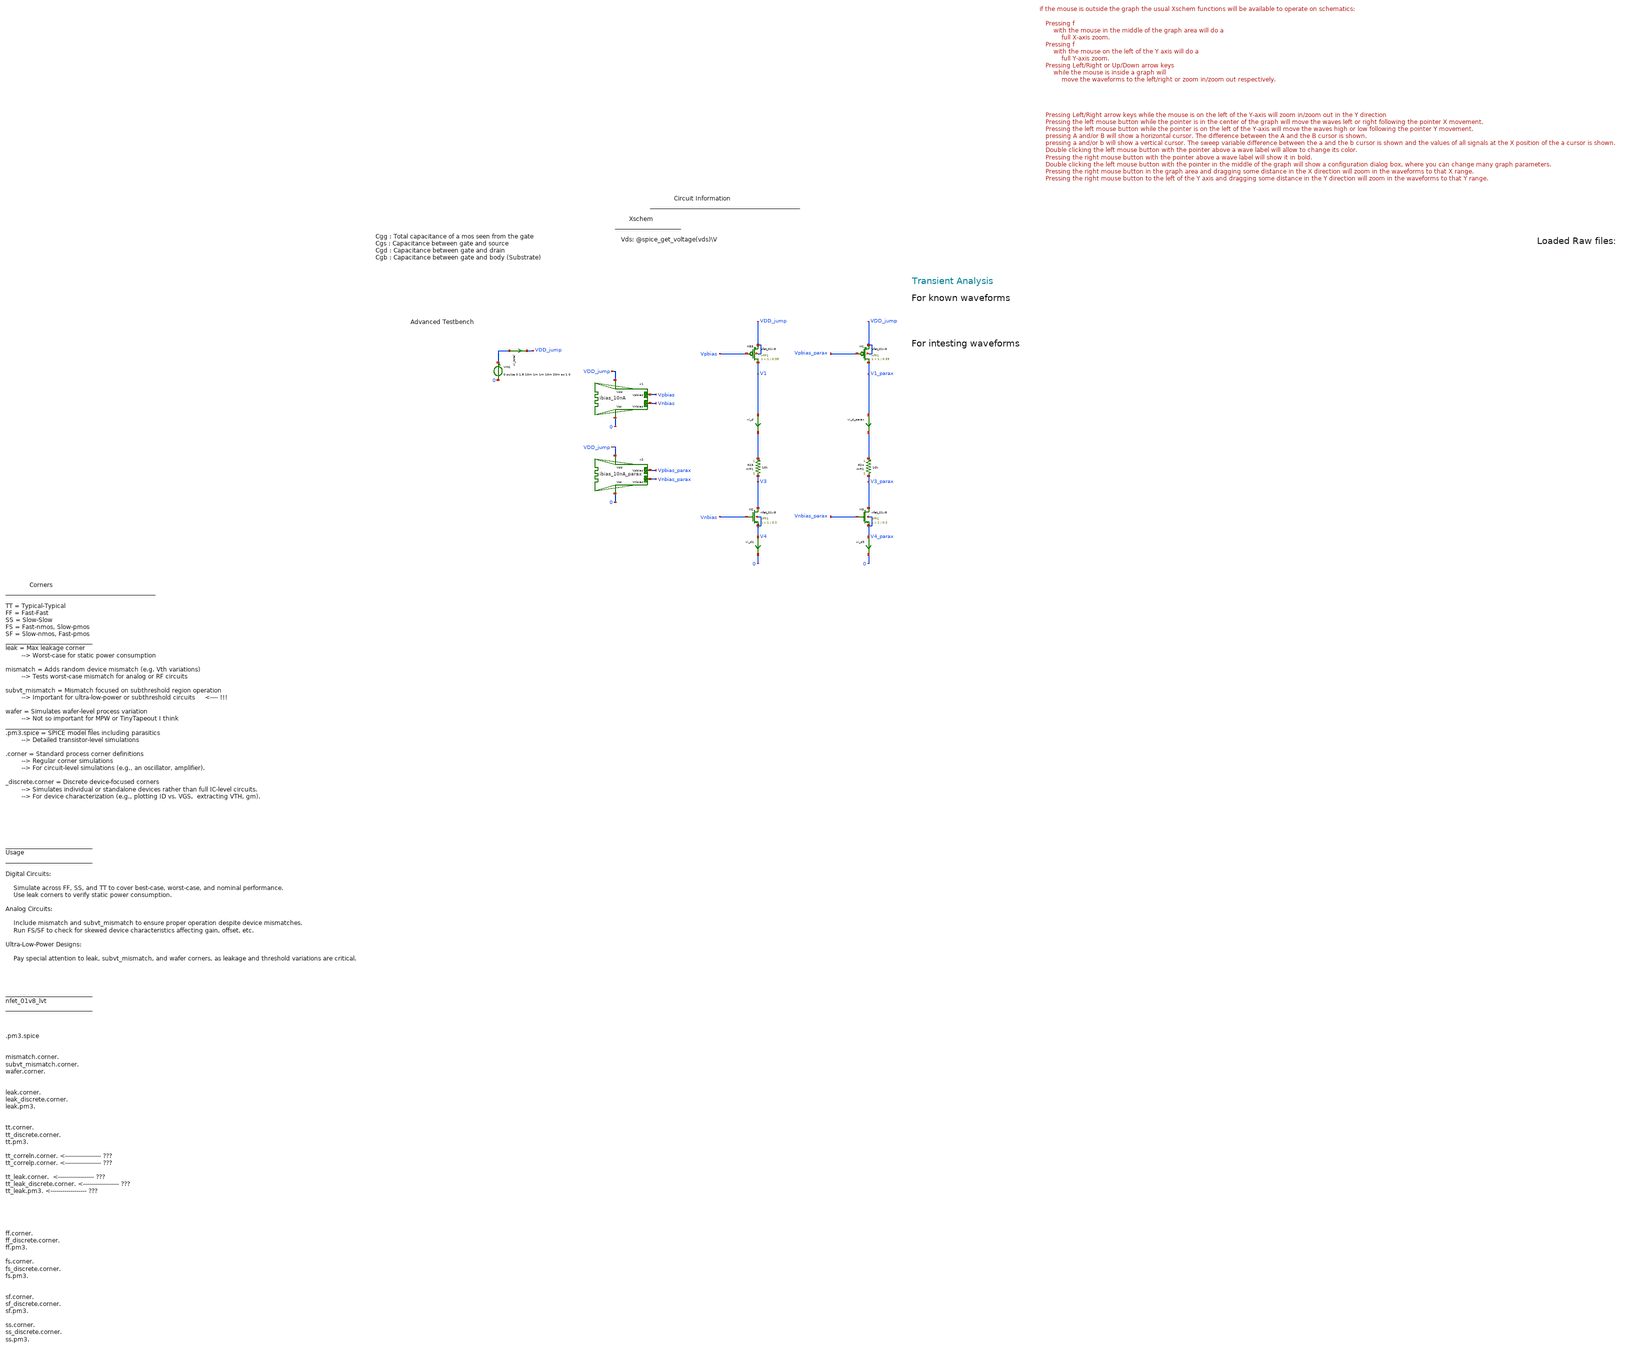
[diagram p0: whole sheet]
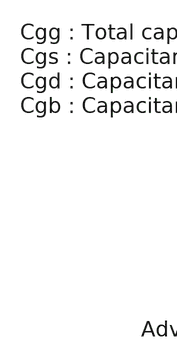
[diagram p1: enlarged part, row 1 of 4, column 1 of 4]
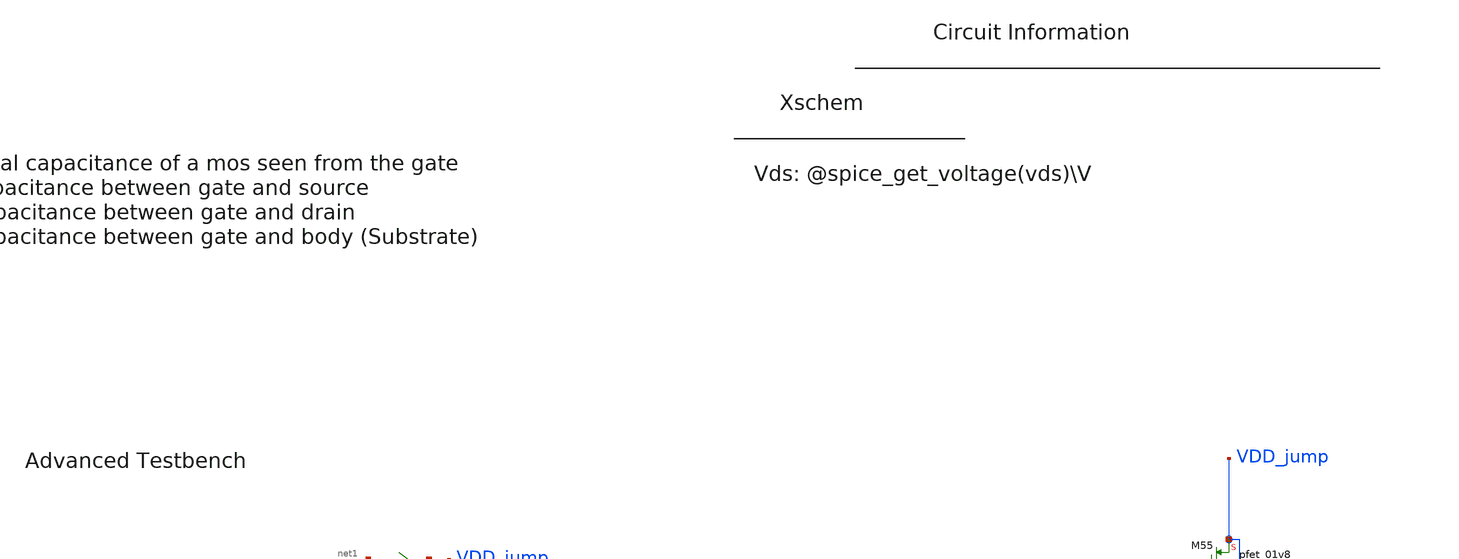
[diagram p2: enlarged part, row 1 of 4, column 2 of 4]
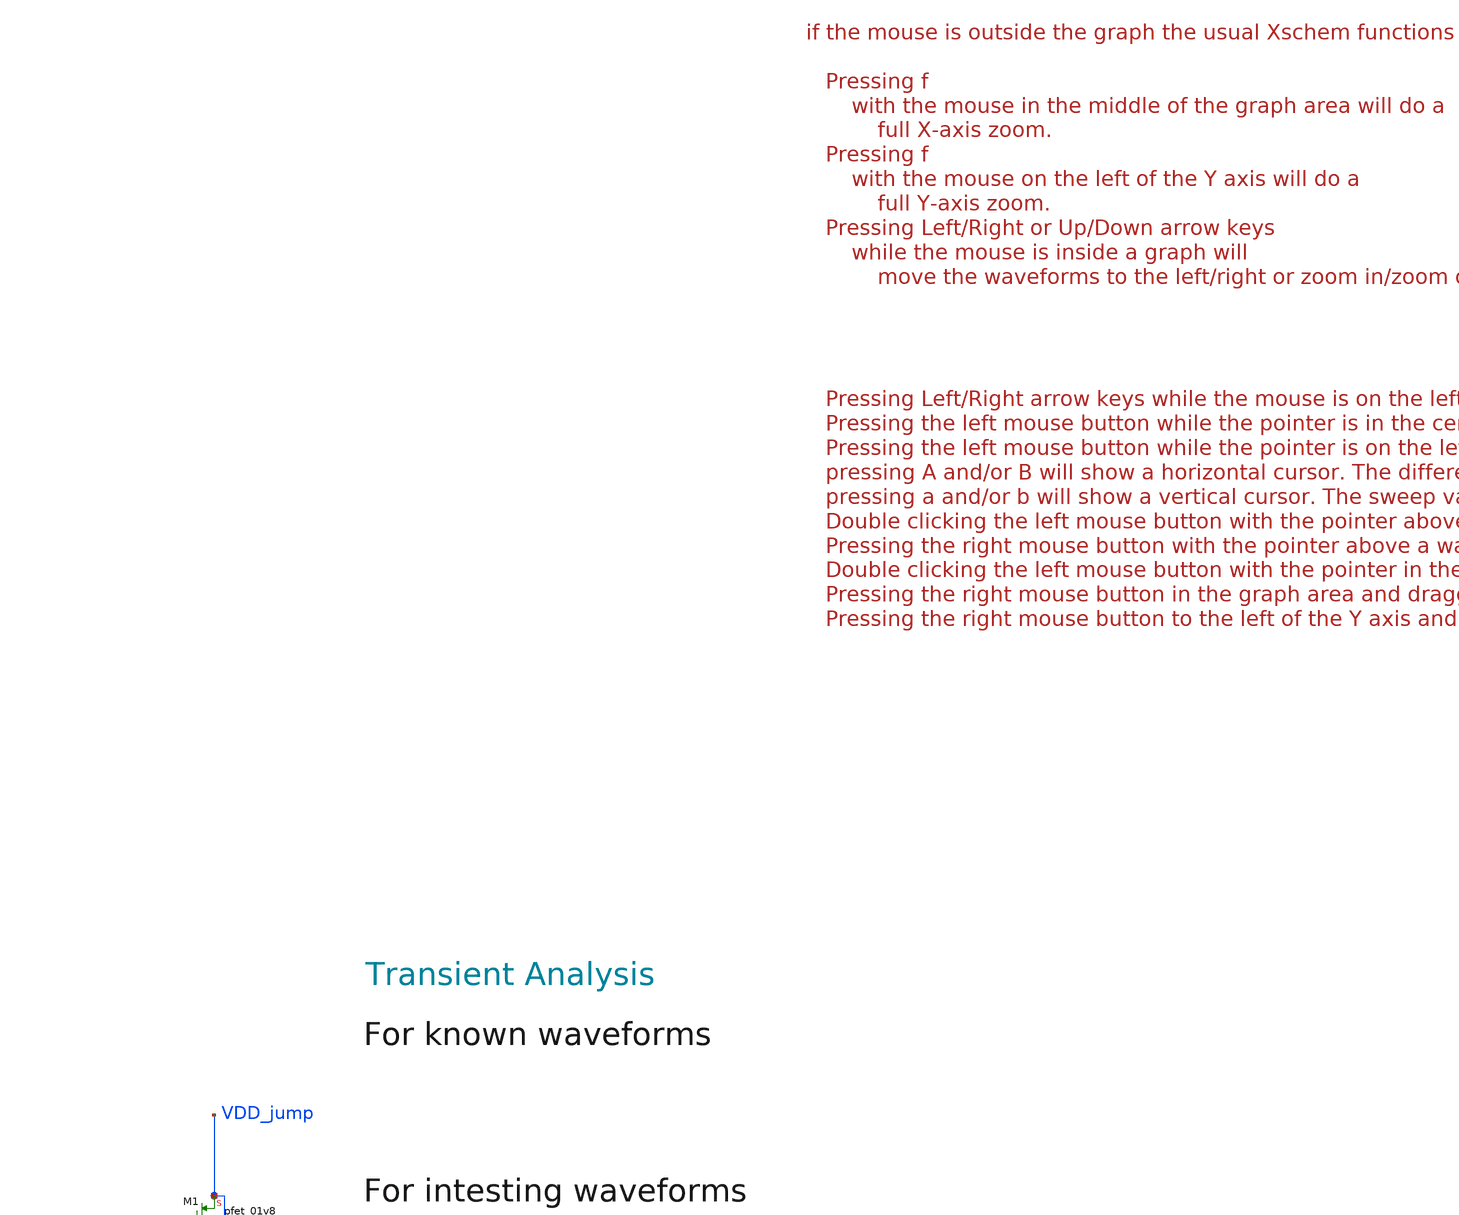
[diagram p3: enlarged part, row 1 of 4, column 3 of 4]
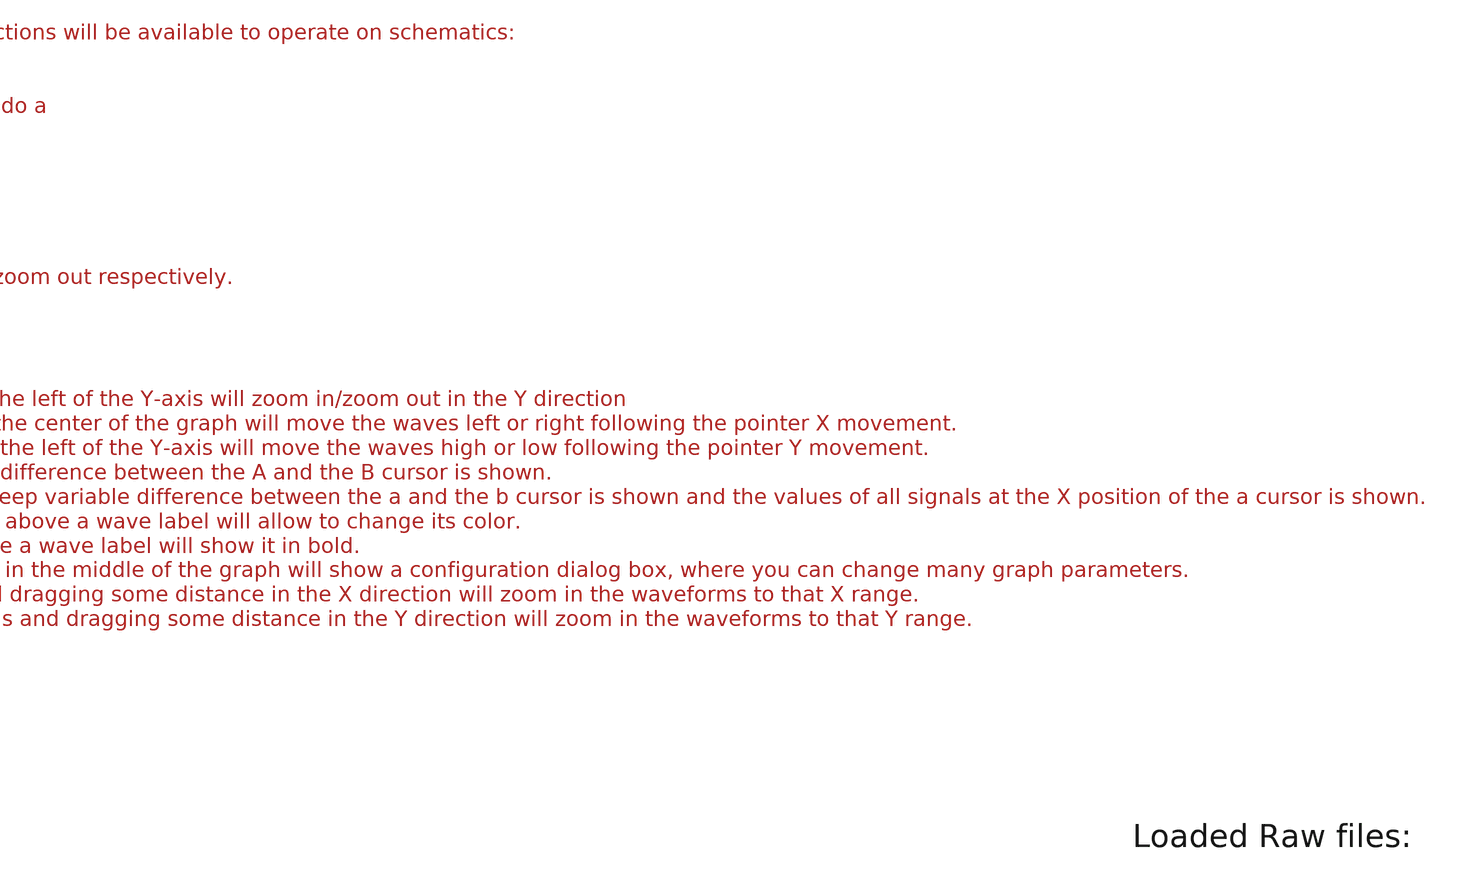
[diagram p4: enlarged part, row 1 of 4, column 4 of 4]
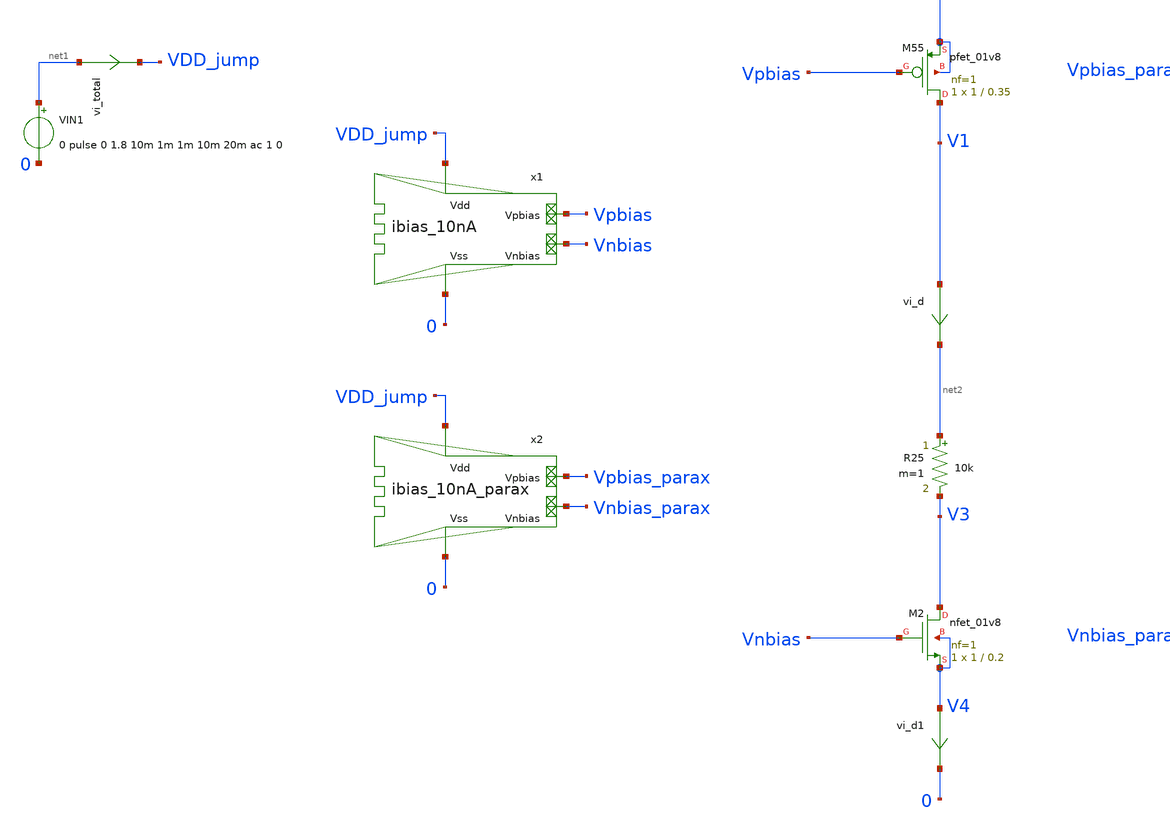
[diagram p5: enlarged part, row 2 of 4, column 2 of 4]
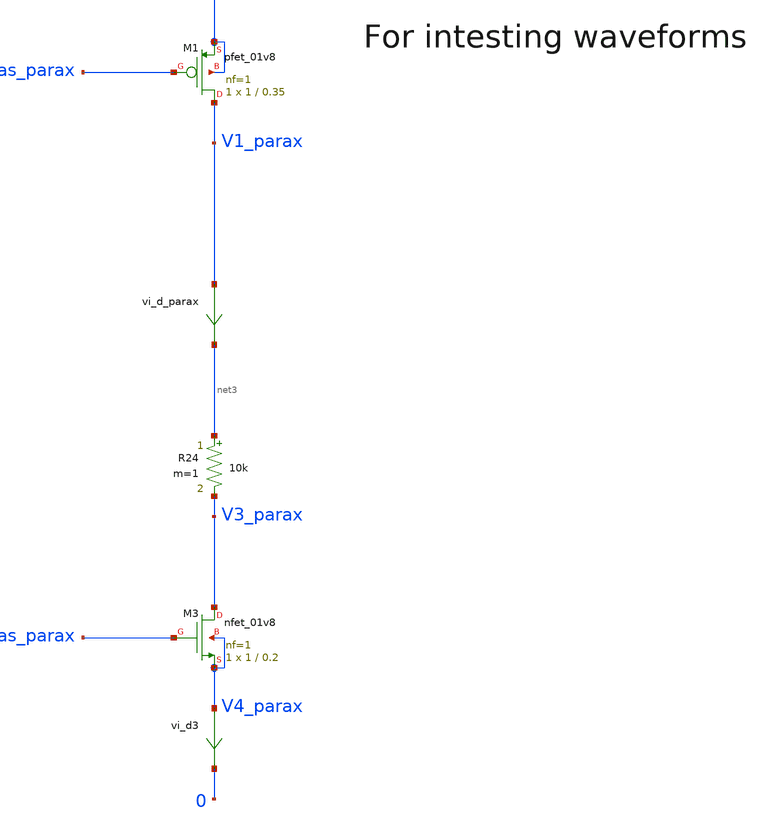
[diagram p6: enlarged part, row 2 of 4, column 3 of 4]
** sch_path: tt10-hdl/tt_um_test_commit/xschem/T2/biasGen/A_tt10_10nA/ibias_10nA_PARAX_tran_tb.sch
* Copyright (C) 1998-2024 Stefan Frederik Schippers
* This program is free software; you can redistribute it and/or modify
* it under the terms of the GNU General Public License as published by
* the Free Software Foundation; either version 2 of the License, or
* (at your option) any later version.
* This program is distributed in the hope that it will be useful,
* but WITHOUT ANY WARRANTY; without even the implied warranty of
* MERCHANTABILITY or FITNESS FOR A PARTICULAR PURPOSE.  See the
* GNU General Public License for more details.
* You should have received a copy of the GNU General Public License
* along with this program; if not, write to the Free Software
**.subckt ibias_10nA_PARAX_tran_tb
VIN1 net1 0 0 pulse 0 1.8 10m 1m 1m 10m 20m ac 1 0
vi_total net1 VDD_jump 0
.save i(vi_total)
vi_d V1 net2 0
.save i(vi_d)
x1 VDD_jump 0 Vnbias Vpbias ibias_10nA
XM55 V1 Vpbias VDD_jump VDD_jump sky130_fd_pr__pfet_01v8 L=0.35 W=1 nf=1 ad='int((nf+1)/2) * W/nf * 0.29'
+ as='int((nf+2)/2) * W/nf * 0.29' pd='2*int((nf+1)/2) * (W/nf + 0.29)' ps='2*int((nf+2)/2) * (W/nf + 0.29)'
+ nrd='0.29 / W' nrs='0.29 / W' sa=0 sb=0 sd=0 mult=1 m=1
R25 net2 V3 10k m=1
XM2 V3 Vnbias V4 V4 sky130_fd_pr__nfet_01v8 L=0.2 W=1 nf=1 ad='int((1 + 1)/2) * 1 / 1 * 0.29' as='int((1 + 2)/2) * 1 / 1 * 0.29'
+ pd='2*int((1 + 1)/2) * (1 / 1 + 0.29)' ps='2*int((1 + 2)/2) * (1 / 1 + 0.29)' nrd='0.29 / 1 ' nrs='0.29 / 1 '
+ sa=0 sb=0 sd=0 mult=1 m=1
vi_d1 V4 0 0
.save i(vi_d1)
vi_d_parax V1_parax net3 0
.save i(vi_d_parax)
XM1 V1_parax Vpbias_parax VDD_jump VDD_jump sky130_fd_pr__pfet_01v8 L=0.35 W=1 nf=1 ad='int((nf+1)/2) * W/nf * 0.29'
+ as='int((nf+2)/2) * W/nf * 0.29' pd='2*int((nf+1)/2) * (W/nf + 0.29)' ps='2*int((nf+2)/2) * (W/nf + 0.29)'
+ nrd='0.29 / W' nrs='0.29 / W' sa=0 sb=0 sd=0 mult=1 m=1
R24 net3 V3_parax 10k m=1
XM3 V3_parax Vnbias_parax V4_parax V4_parax sky130_fd_pr__nfet_01v8 L=0.2 W=1 nf=1 ad='int((1 + 1)/2) * 1 / 1 * 0.29'
+ as='int((1 + 2)/2) * 1 / 1 * 0.29' pd='2*int((1 + 1)/2) * (1 / 1 + 0.29)' ps='2*int((1 + 2)/2) * (1 / 1 + 0.29)'
+ nrd='0.29 / 1 ' nrs='0.29 / 1 ' sa=0 sb=0 sd=0 mult=1 m=1
vi_d3 V4_parax 0 0
.save i(vi_d3)
x2 VDD_jump 0 Vnbias_parax Vpbias_parax ibias_10nA_parax
**** begin user architecture code



.temp 30

*.option gmin=5n
*.option scale=1e-6
.option wnflag=1
.option savecurrents

.save all
.control
  save all alli
  save @m.xm1.msky130_fd_pr__nfet_01v8[gm]
  save @m.xm1.msky130_fd_pr__nfet_01v8[id]
  save @m.xm1.msky130_fd_pr__nfet_01v8[vgs]

  save @m.xm1.msky130_fd_pr__nfet_01v8[cgg]
  save @m.xm1.msky130_fd_pr__nfet_01v8[cgs]
  save @m.xm1.msky130_fd_pr__nfet_01v8[cgdo]
  save @m.xm1.msky130_fd_pr__nfet_01v8[cgb]

  save @m.xm1.msky130_fd_pr__nfet_01v8[vds]
  save @m.xm1.msky130_fd_pr__nfet_01v8[vdsat]
  save @m.xm1.msky130_fd_pr__nfet_01v8[vth]


  save @m.xm1.msky130_fd_pr__nfet_01v8[leff]
  save @m.xm1.msky130_fd_pr__nfet_01v8[weff]
  save @m.xm1.msky130_fd_pr__nfet_01v8[gds]
  save @m.xm1.msky130_fd_pr__nfet_01v8[l]
  save @m.xm1.msky130_fd_pr__nfet_01v8[w]
  save @m.xm1.msky130_fd_pr__nfet_01v8[gm]
  save @m.xm1.msky130_fd_pr__nfet_01v8[gm]
  save @m.xm1.msky130_fd_pr__nfet_01v8[gm]
  save @m.xm1.msky130_fd_pr__nfet_01v8[gm]
  save @m.xm1.msky130_fd_pr__nfet_01v8[gm]








  tran 1m 50m
  remzerovec
  write nmos_tb_tran.raw

  op
  set appendwrite
  remzerovec
  write nmos_tb_tran.raw






  *quit 0




.endc





** opencircuitdesign pdks install
.lib $::SKYWATER_MODELS/sky130.lib.spice tt
.include $::SKYWATER_STDCELLS/sky130_fd_sc_hd.spice


**** end user architecture code
**.ends

* expanding   symbol:  T2/biasGen/A_tt10_10nA/ibias_10nA.sym # of pins=4
** sym_path: tt10-hdl/tt_um_test_commit/xschem/T2/biasGen/A_tt10_10nA/ibias_10nA.sym
** sch_path: tt10-hdl/tt_um_test_commit/xschem/T2/biasGen/A_tt10_10nA/ibias_10nA.sch
.subckt ibias_10nA Vdd Vss Vnbias Vpbias
*.ipin Vdd
*.ipin Vss
*.opin Vnbias
*.opin Vpbias
XM3 Vpbias Vpbias Vdd Vdd sky130_fd_pr__pfet_01v8 L=0.35 W=0.5 nf=1 ad='int((nf+1)/2) * W/nf * 0.29'
+ as='int((nf+2)/2) * W/nf * 0.29' pd='2*int((nf+1)/2) * (W/nf + 0.29)' ps='2*int((nf+2)/2) * (W/nf + 0.29)'
+ nrd='0.29 / W' nrs='0.29 / W' sa=0 sb=0 sd=0 mult=1 m=1
XM4 Vnbias Vpbias Vdd Vdd sky130_fd_pr__pfet_01v8 L=0.35 W=0.5 nf=1 ad='int((nf+1)/2) * W/nf * 0.29'
+ as='int((nf+2)/2) * W/nf * 0.29' pd='2*int((nf+1)/2) * (W/nf + 0.29)' ps='2*int((nf+2)/2) * (W/nf + 0.29)'
+ nrd='0.29 / W' nrs='0.29 / W' sa=0 sb=0 sd=0 mult=1 m=1
XM5 net2 Vpbias Vdd Vdd sky130_fd_pr__pfet_01v8 L=0.35 W=1 nf=1 ad='int((nf+1)/2) * W/nf * 0.29' as='int((nf+2)/2) * W/nf * 0.29'
+ pd='2*int((nf+1)/2) * (W/nf + 0.29)' ps='2*int((nf+2)/2) * (W/nf + 0.29)' nrd='0.29 / W' nrs='0.29 / W'
+ sa=0 sb=0 sd=0 mult=1 m=1
XM1 Vpbias Vnbias net1 Vss sky130_fd_pr__nfet_01v8 L=0.2 W=0.5 nf=1 ad='int((1 + 1)/2) * 0.5 / 1 * 0.29'
+ as='int((1 + 2)/2) * 0.5 / 1 * 0.29' pd='2*int((1 + 1)/2) * (0.5 / 1 + 0.29)' ps='2*int((1 + 2)/2) * (0.5 / 1 + 0.29)'
+ nrd='0.29 / 0.5 ' nrs='0.29 / 0.5 ' sa=0 sb=0 sd=0 mult=1 m=1
XM2 Vnbias Vnbias Vss Vss sky130_fd_pr__nfet_01v8 L=0.2 W=0.5 nf=1 ad='int((1 + 1)/2) * 0.5 / 1 * 0.29'
+ as='int((1 + 2)/2) * 0.5 / 1 * 0.29' pd='2*int((1 + 1)/2) * (0.5 / 1 + 0.29)' ps='2*int((1 + 2)/2) * (0.5 / 1 + 0.29)'
+ nrd='0.29 / 0.5 ' nrs='0.29 / 0.5 ' sa=0 sb=0 sd=0 mult=1 m=1
XM6 net2 net2 net1 Vss sky130_fd_pr__nfet_01v8 L=0.2 W=1 nf=1 ad='int((1 + 1)/2) * 1 / 1 * 0.29' as='int((1 + 2)/2) * 1 / 1 * 0.29'
+ pd='2*int((1 + 1)/2) * (1 / 1 + 0.29)' ps='2*int((1 + 2)/2) * (1 / 1 + 0.29)' nrd='0.29 / 1 ' nrs='0.29 / 1 '
+ sa=0 sb=0 sd=0 mult=1 m=1
XM7 net1 net2 Vss Vss sky130_fd_pr__nfet_01v8 L=1 W=1 nf=1 ad='int((1 + 1)/2) * 1 / 1 * 0.29' as='int((1 + 2)/2) * 1 / 1 * 0.29'
+ pd='2*int((1 + 1)/2) * (1 / 1 + 0.29)' ps='2*int((1 + 2)/2) * (1 / 1 + 0.29)' nrd='0.29 / 1 ' nrs='0.29 / 1 '
+ sa=0 sb=0 sd=0 mult=1 m=1
.ends


* expanding   symbol:  T2/biasGen/A_tt10_10nA/ibias_10nA_parax.sym # of pins=4
** sym_path: tt10-hdl/tt_um_test_commit/xschem/T2/biasGen/A_tt10_10nA/ibias_10nA_parax.sym
.include T2/biasGen/A_tt10_10nA/ibias_10nA_parax.spice
.end
